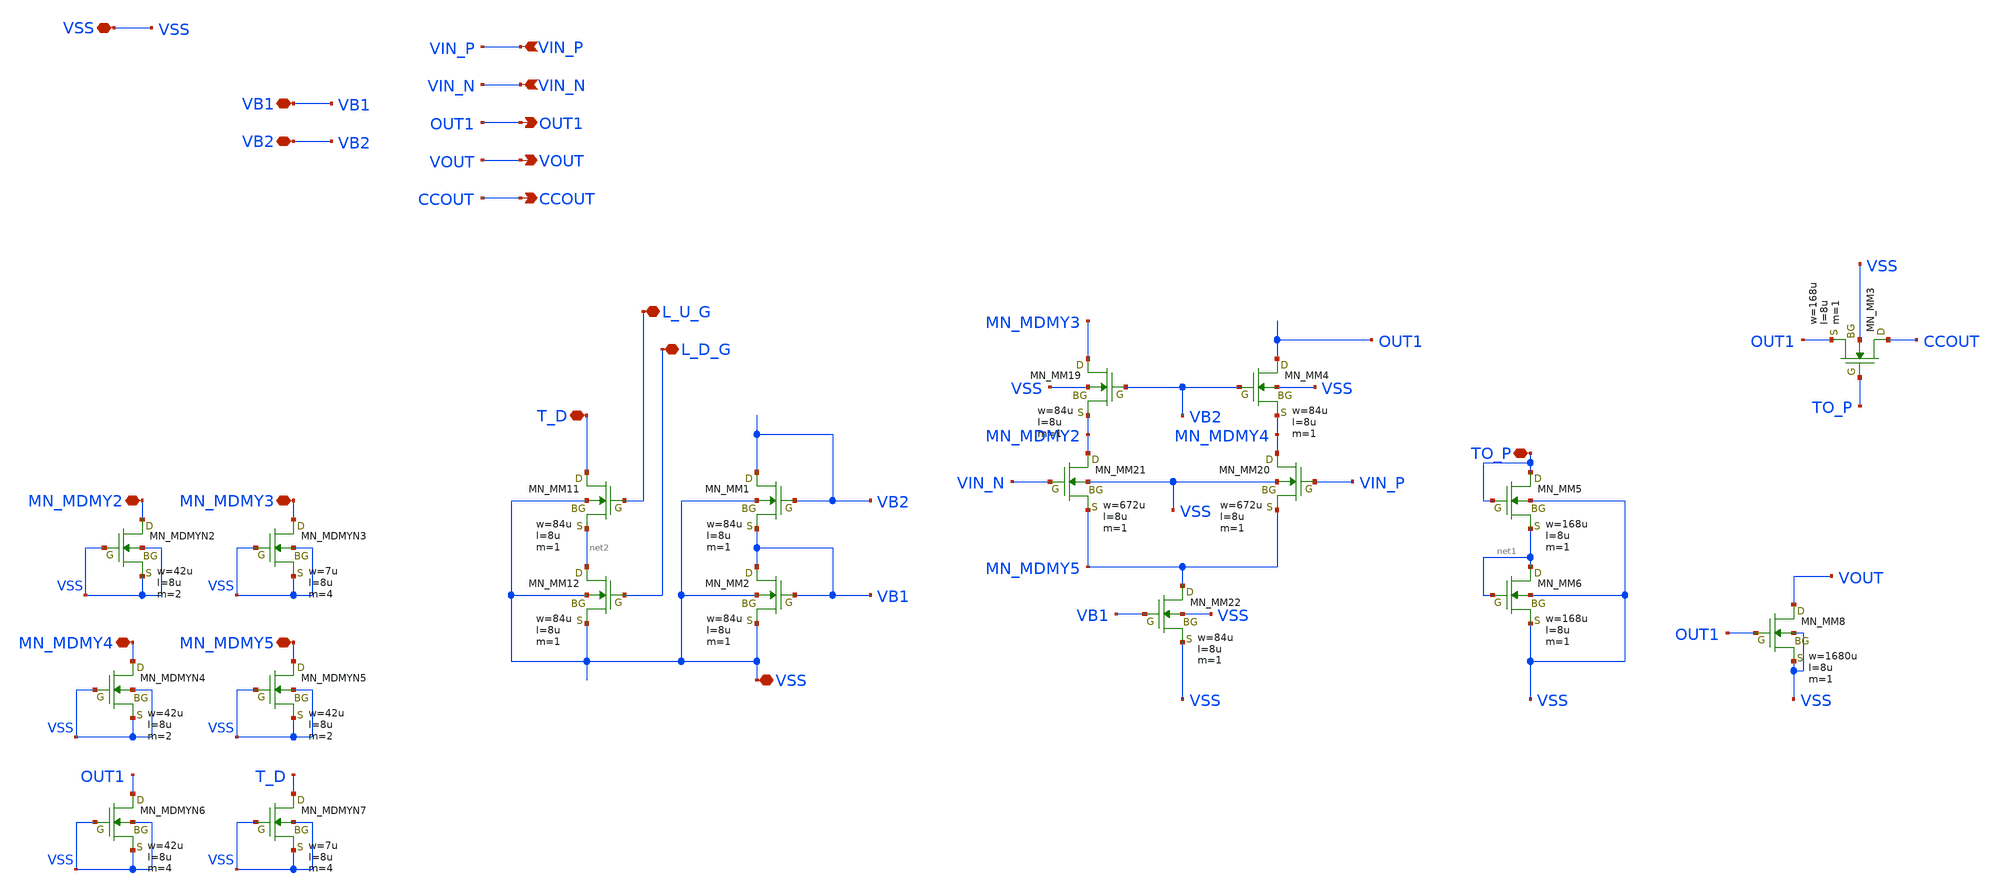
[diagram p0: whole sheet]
** sch_path: member_project/AM_Radio/noritsuna/xschem/OPAMP_NMOS_single.sch
**.subckt OPAMP_NMOS_single VSS VB1 VB2 OUT1 VIN_N VIN_P MN_MDMY2 MN_MDMY3 MN_MDMY4 TO_P MN_MDMY5
*+ VOUT CCOUT VSS L_U_G L_D_G T_D
*.iopin VSS
*.iopin VB1
*.iopin VB2
*.opin OUT1
*.ipin VIN_N
*.ipin VIN_P
*.iopin MN_MDMY2
*.iopin MN_MDMY3
*.iopin MN_MDMY4
*.iopin TO_P
*.iopin MN_MDMY5
*.opin VOUT
*.opin CCOUT
*.iopin VSS
*.iopin L_U_G
*.iopin L_D_G
*.iopin T_D
MM4 OUT1 VB2 MN_MDMY4 VSS NMOS w=84u l=8u as=0 ad=0 ps=0 pd=0 nrd=0 nrs=0 m=1
MM19 MN_MDMY3 VB2 MN_MDMY2 VSS NMOS w=84u l=8u as=0 ad=0 ps=0 pd=0 nrd=0 nrs=0 m=1
MM20 MN_MDMY4 VIN_P MN_MDMY5 VSS NMOS w=672u l=8u as=0 ad=0 ps=0 pd=0 nrd=0 nrs=0 m=1
MM21 MN_MDMY2 VIN_N MN_MDMY5 VSS NMOS w=672u l=8u as=0 ad=0 ps=0 pd=0 nrd=0 nrs=0 m=1
MM22 MN_MDMY5 VB1 VSS VSS NMOS w=84u l=8u as=0 ad=0 ps=0 pd=0 nrd=0 nrs=0 m=1
XMDMYN2 MN_MDMY2 VSS VSS VSS NMOS w=42u l=8u as=0 ad=0 ps=0 pd=0 nrd=0 nrs=0 m=2
XMDMYN3 MN_MDMY3 VSS VSS VSS NMOS w=7u l=8u as=0 ad=0 ps=0 pd=0 nrd=0 nrs=0 m=4
MM6 net1 net1 VSS VSS NMOS w=168u l=8u as=0 ad=0 ps=0 pd=0 nrd=0 nrs=0 m=1
MM5 TO_P TO_P net1 VSS NMOS w=168u l=8u as=0 ad=0 ps=0 pd=0 nrd=0 nrs=0 m=1
XMDMYN4 MN_MDMY4 VSS VSS VSS NMOS w=42u l=8u as=0 ad=0 ps=0 pd=0 nrd=0 nrs=0 m=2
XMDMYN5 MN_MDMY5 VSS VSS VSS NMOS w=42u l=8u as=0 ad=0 ps=0 pd=0 nrd=0 nrs=0 m=2
MM8 VOUT OUT1 VSS VSS NMOS w=1680u l=8u as=0 ad=0 ps=0 pd=0 nrd=0 nrs=0 m=1
MM3 CCOUT TO_P OUT1 VSS NMOS w=168u l=8u as=0 ad=0 ps=0 pd=0 nrd=0 nrs=0 m=1
XMDMYN6 OUT1 VSS VSS VSS NMOS w=42u l=8u as=0 ad=0 ps=0 pd=0 nrd=0 nrs=0 m=4
MM1 VB2 VB2 VB1 VSS NMOS w=84u l=8u as=0 ad=0 ps=0 pd=0 nrd=0 nrs=0 m=1
MM2 VB1 VB1 VSS VSS NMOS w=84u l=8u as=0 ad=0 ps=0 pd=0 nrd=0 nrs=0 m=1
MM11 T_D L_U_G net2 VSS NMOS w=84u l=8u as=0 ad=0 ps=0 pd=0 nrd=0 nrs=0 m=1
MM12 net2 L_D_G VSS VSS NMOS w=84u l=8u as=0 ad=0 ps=0 pd=0 nrd=0 nrs=0 m=1
XMDMYN7 T_D VSS VSS VSS NMOS w=7u l=8u as=0 ad=0 ps=0 pd=0 nrd=0 nrs=0 m=4
**.ends
.end
